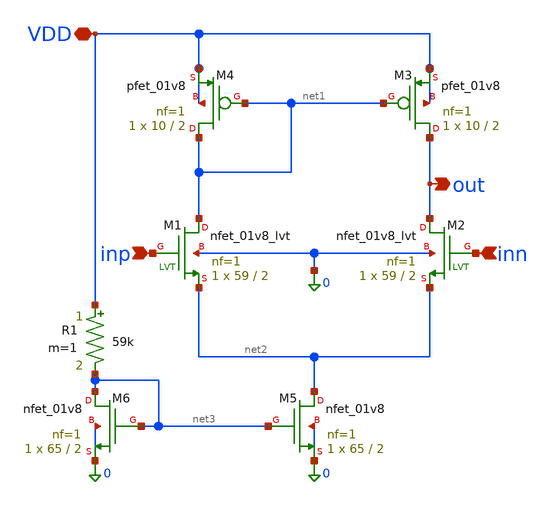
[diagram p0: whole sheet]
** sch_path: bandgap_ota.sch
**.subckt bandgap_ota VDD inp inn out
*.iopin VDD
*.ipin inp
*.ipin inn
*.opin out
XM1 net1 inp net2 0 sky130_fd_pr__nfet_01v8_lvt L=2 W=59 nf=1 ad='int((1 + 1)/2) * 59 / 1 * 0.29' as='int((1 + 2)/2) * 59 / 1 * 0.29'
+ pd='2*int((1 + 1)/2) * (59 / 1 + 0.29)' ps='2*int((1 + 2)/2) * (59 / 1 + 0.29)' nrd='0.29 / 59 ' nrs='0.29 / 59 '
+ sa=0 sb=0 sd=0 mult=1 m=1
XM2 out inn net2 0 sky130_fd_pr__nfet_01v8_lvt L=2 W=59 nf=1 ad='int((1 + 1)/2) * 59 / 1 * 0.29' as='int((1 + 2)/2) * 59 / 1 * 0.29'
+ pd='2*int((1 + 1)/2) * (59 / 1 + 0.29)' ps='2*int((1 + 2)/2) * (59 / 1 + 0.29)' nrd='0.29 / 59 ' nrs='0.29 / 59 '
+ sa=0 sb=0 sd=0 mult=1 m=1
XM3 out net1 VDD VDD sky130_fd_pr__pfet_01v8 L=2 W=10 nf=1 ad='int((1 + 1)/2) * 10 / 1 * 0.29' as='int((1 + 2)/2) * 10 / 1 * 0.29'
+ pd='2*int((1 + 1)/2) * (10 / 1 + 0.29)' ps='2*int((1 + 2)/2) * (10 / 1 + 0.29)' nrd='0.29 / 10 ' nrs='0.29 / 10 '
+ sa=0 sb=0 sd=0 mult=1 m=1
XM4 net1 net1 VDD VDD sky130_fd_pr__pfet_01v8 L=2 W=10 nf=1 ad='int((1 + 1)/2) * 10 / 1 * 0.29' as='int((1 + 2)/2) * 10 / 1 * 0.29'
+ pd='2*int((1 + 1)/2) * (10 / 1 + 0.29)' ps='2*int((1 + 2)/2) * (10 / 1 + 0.29)' nrd='0.29 / 10 ' nrs='0.29 / 10 '
+ sa=0 sb=0 sd=0 mult=1 m=1
XM5 net2 net3 0 0 sky130_fd_pr__nfet_01v8 L=2 W=65 nf=1 ad='int((1 + 1)/2) * 65 / 1 * 0.29' as='int((1 + 2)/2) * 65 / 1 * 0.29'
+ pd='2*int((1 + 1)/2) * (65 / 1 + 0.29)' ps='2*int((1 + 2)/2) * (65 / 1 + 0.29)' nrd='0.29 / 65 ' nrs='0.29 / 65 '
+ sa=0 sb=0 sd=0 mult=1 m=1
XM6 net3 net3 0 0 sky130_fd_pr__nfet_01v8 L=2 W=65 nf=1 ad='int((1 + 1)/2) * 65 / 1 * 0.29' as='int((1 + 2)/2) * 65 / 1 * 0.29'
+ pd='2*int((1 + 1)/2) * (65 / 1 + 0.29)' ps='2*int((1 + 2)/2) * (65 / 1 + 0.29)' nrd='0.29 / 65 ' nrs='0.29 / 65 '
+ sa=0 sb=0 sd=0 mult=1 m=1
R1 VDD net3 59k m=1
**.ends
.end
